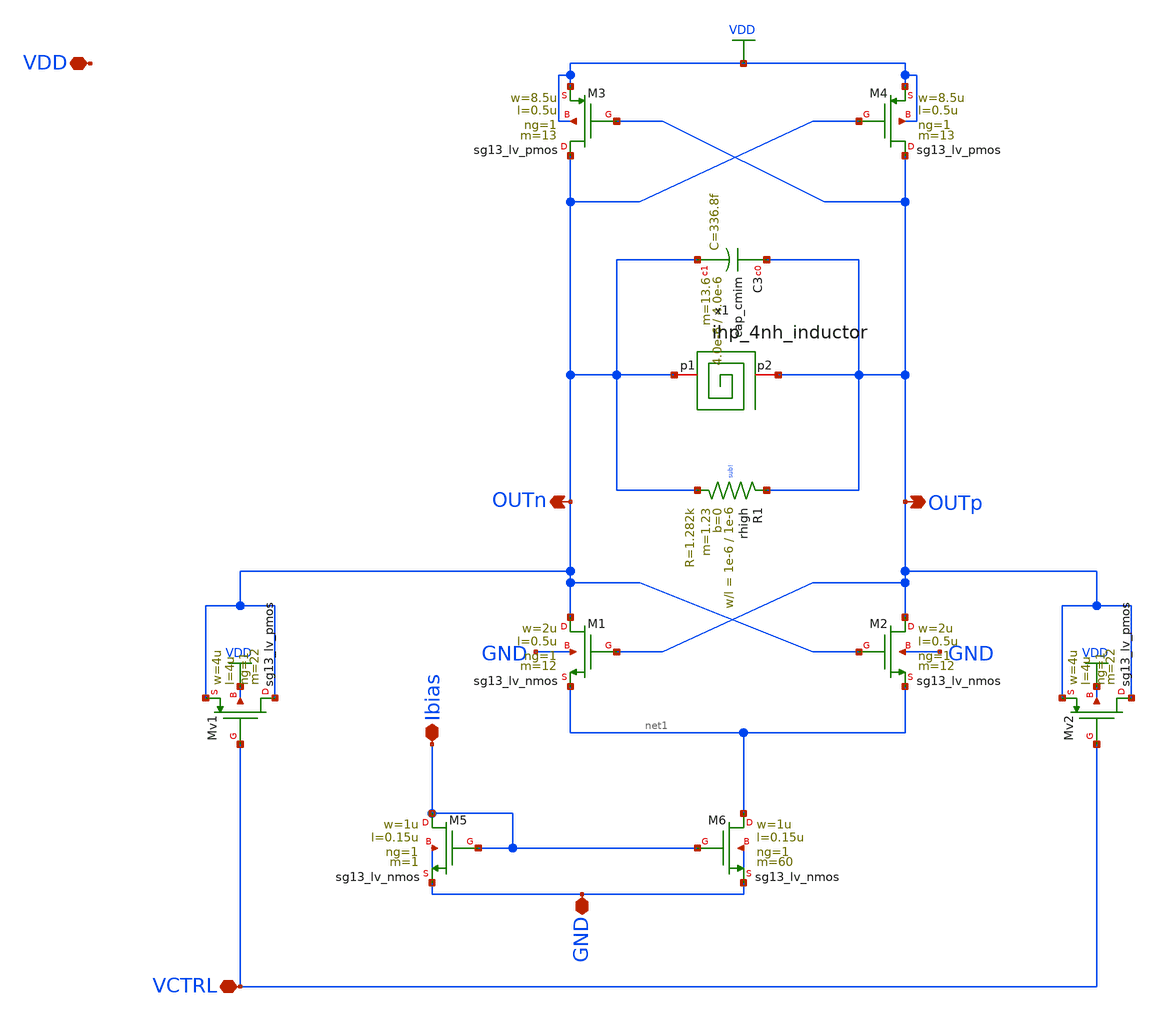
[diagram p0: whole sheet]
** sch_path: schematic/blocks/top-pll/lc-vco/LC_VCO.sch
**.subckt LC_VCO VDD OUTp OUTn GND VCTRL Ibias
*.iopin VDD
*.opin OUTp
*.opin OUTn
*.iopin GND
*.iopin VCTRL
*.iopin Ibias
XM6 net1 Ibias GND GND sg13_lv_nmos w=1u l=0.15u ng=1 m=60 mm_ok=1
XM5 Ibias Ibias GND GND sg13_lv_nmos w=1u l=0.15u ng=1 m=1 mm_ok=1
XM4 OUTp OUTn VDD VDD sg13_lv_pmos w=8.5u l=0.5u ng=1 m=13 mm_ok=1
X5M3 OUTn OUTp VDD VDD sg13_lv_pmos w=8.5u l=0.5u ng=1 m=13 mm_ok=1
XM2 OUTp OUTn net1 GND sg13_lv_nmos w=2u l=0.5u ng=1 m=12 mm_ok=1
XM1 OUTn OUTp net1 GND sg13_lv_nmos w=2u l=0.5u ng=1 m=12 mm_ok=1
XC3 OUTp OUTn cap_cmim w=4.0e-6 l=4.0e-6 m=13.6 mm_ok=1
XMv2 OUTp VCTRL OUTp VDD sg13_lv_pmos w=4u l=4u ng=1 m=22 mm_ok=1
XMv1 OUTn VCTRL OUTn VDD sg13_lv_pmos w=4u l=4u ng=1 m=22 mm_ok=1
XR1 OUTp OUTn sub! rhigh w=1e-6 l=1e-6 m=1.23 b=0 mm_ok=1
x1 OUTn OUTp ihp_4nh_inductor
**.ends
.GLOBAL VDD
.end
